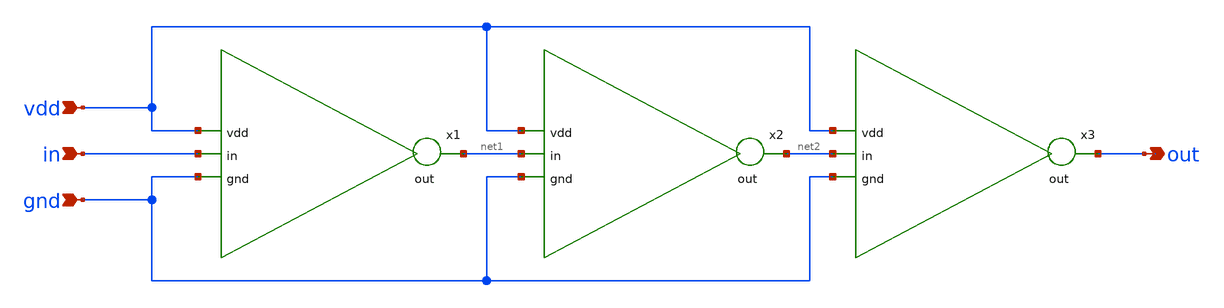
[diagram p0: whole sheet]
** sch_path: Inverter/untitled.sch
**.subckt untitled out vdd in gnd
*.opin out
*.ipin vdd
*.ipin in
*.ipin gnd
x1 vdd net1 in gnd inverter
x2 vdd net2 net1 gnd inverter
x3 vdd out net2 gnd inverter
**.ends
.end
